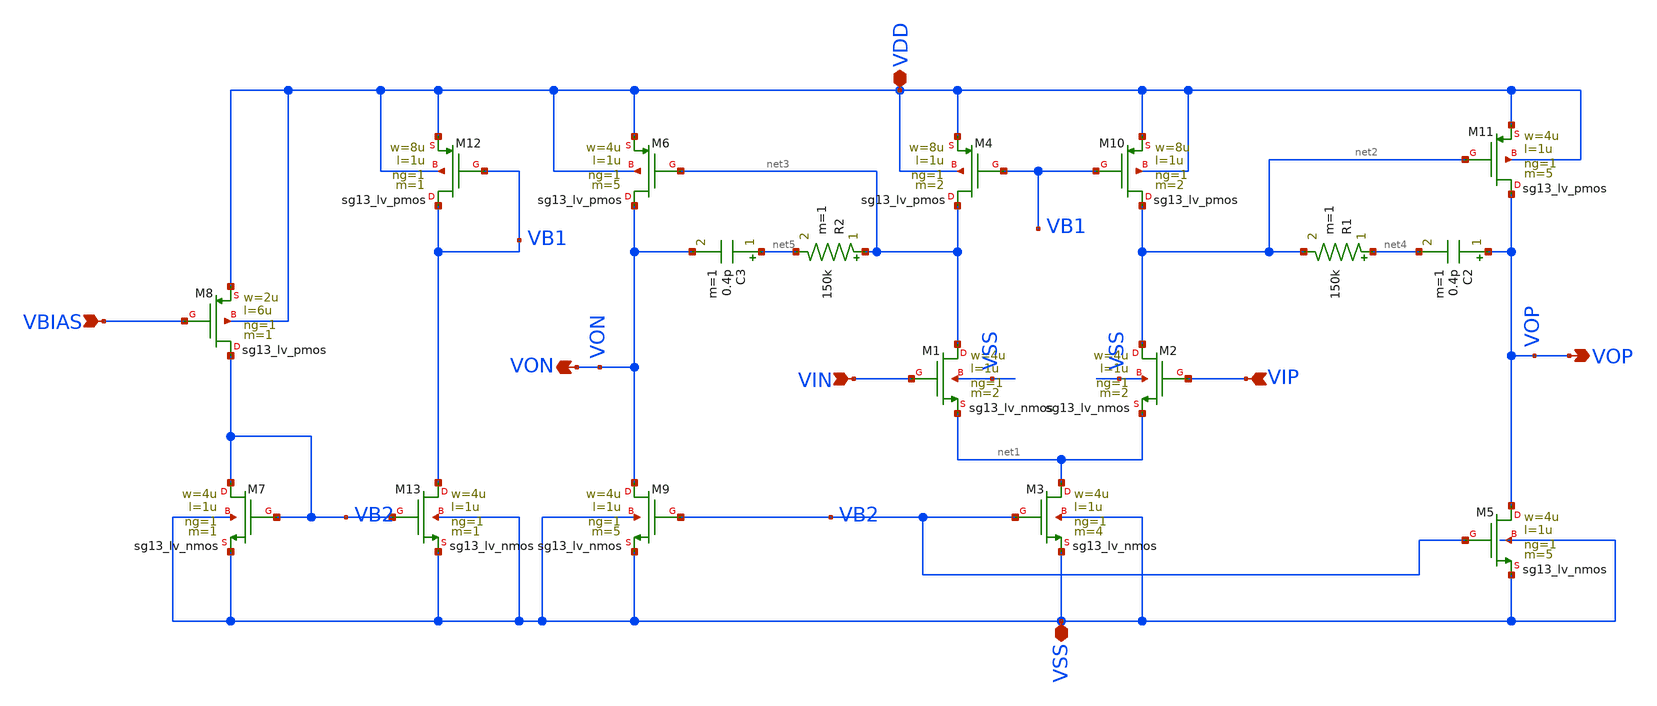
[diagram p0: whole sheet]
** sch_path: BTDay5-Ex/full-diff_2-stage-OpampCore.sch
**.subckt full-diff_2-stage-OpampCore VIN VIP VOP VDD VSS VBIAS VON
*.ipin VIN
*.ipin VIP
*.opin VOP
*.iopin VDD
*.iopin VSS
*.ipin VBIAS
*.opin VON
XM1 net3 VIN net1 VSS sg13_lv_nmos w=4u l=1u ng=1 m=2 mm_ok=1
XM2 net2 VIP net1 VSS sg13_lv_nmos w=4u l=1u ng=1 m=2 mm_ok=1
XM3 net1 VB2 VSS VSS sg13_lv_nmos w=4u l=1u ng=1 m=4 mm_ok=1
XM4 net3 VB1 VDD VDD sg13_lv_pmos w=8u l=1u ng=1 m=2 mm_ok=1
XM7 VB2 VB2 VSS VSS sg13_lv_nmos w=4u l=1u ng=1 m=1 mm_ok=1
XM8 VB2 VBIAS VDD VDD sg13_lv_pmos w=2u l=6u ng=1 m=1 mm_ok=1
XM10 net2 VB1 VDD VDD sg13_lv_pmos w=8u l=1u ng=1 m=2 mm_ok=1
XM5 VOP VB2 VSS VSS sg13_lv_nmos w=4u l=1u ng=1 m=5 mm_ok=1
XM11 VOP net2 VDD VDD sg13_lv_pmos w=4u l=1u ng=1 m=5 mm_ok=1
C2 VOP net4 0.4p m=1
R1 net4 net2 150k m=1
XM9 VON VB2 VSS VSS sg13_lv_nmos w=4u l=1u ng=1 m=5 mm_ok=1
C3 net5 VON 0.4p m=1
R2 net3 net5 150k m=1
XM12 VB1 VB1 VDD VDD sg13_lv_pmos w=8u l=1u ng=1 m=1 mm_ok=1
XM13 VB1 VB2 VSS VSS sg13_lv_nmos w=4u l=1u ng=1 m=1 mm_ok=1
XM6 VON net3 VDD VDD sg13_lv_pmos w=4u l=1u ng=1 m=5 mm_ok=1
**.ends
.end
